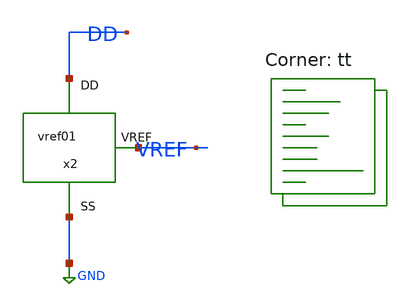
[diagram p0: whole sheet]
** sch_path: xschem/test_vref01.sch
**.subckt test_vref01
x2 VREF DD GND vref01
**** begin user architecture code
.lib $::SKYWATER_MODELS/sky130.lib.spice tt
**** end user architecture code
**.ends

* expanding   symbol:  vref01.sym # of pins=3
** sym_path: xschem/vref01.sym
** sch_path: xschem/vref01.sch
.subckt vref01 VREF DD SS
*.opin VREF
*.iopin SS
*.iopin DD
XM1 DD gate gate SS sky130_fd_pr__nfet_01v8_lvt L=0.89 W=6 nf=1 ad='int((nf+1)/2) * W/nf * 0.29' as='int((nf+2)/2) * W/nf * 0.29'
+ pd='2*int((nf+1)/2) * (W/nf + 0.29)' ps='2*int((nf+2)/2) * (W/nf + 0.29)' nrd='0.29 / W' nrs='0.29 / W'
+ sa=0 sb=0 sd=0 mult=2 m=2
XM2 gate gate VREF SS sky130_fd_pr__nfet_01v8_lvt L=3.10 W=1.72 nf=1 ad='int((nf+1)/2) * W/nf * 0.29'
+ as='int((nf+2)/2) * W/nf * 0.29' pd='2*int((nf+1)/2) * (W/nf + 0.29)' ps='2*int((nf+2)/2) * (W/nf + 0.29)'
+ nrd='0.29 / W' nrs='0.29 / W' sa=0 sb=0 sd=0 mult=1 m=1
XM3 VREF gate SS SS sky130_fd_pr__nfet_01v8 L=1.05 W=0.82 nf=1 ad='int((nf+1)/2) * W/nf * 0.29' as='int((nf+2)/2) * W/nf * 0.29'
+ pd='2*int((nf+1)/2) * (W/nf + 0.29)' ps='2*int((nf+2)/2) * (W/nf + 0.29)' nrd='0.29 / W' nrs='0.29 / W'
+ sa=0 sb=0 sd=0 mult=1 m=1
XM4 VREF VREF VREF DD sky130_fd_pr__pfet_01v8_lvt L=0.35 W=8.6 nf=1 ad='int((nf+1)/2) * W/nf * 1' as='int((nf+2)/2) * W/nf * 1'
+ pd='2*int((nf+1)/2) * (W/nf + 1)' ps='2*int((nf+2)/2) * (W/nf + 1)' nrd='1 / W' nrs='1 / W' sa=0 sb=0
+ sd=0 mult=1 m=1
.ends

.GLOBAL GND
**** begin user architecture code


** this experimental option enables mos model bin
** selection based on W/NF instead of W
*.option wnflag=1 savecurrents
.option gmin=1e-15 reltol=1e-3 vntol=1e-4 abstol=1e-14

.param vdd=1
v1 dd 0 dc=vdd


.control
  option seed = 8
  let run = 1
  save all
  op
  write test_vref01.raw
  reset
  set appendwrite
  dowhile run < = 1
    save vref i(v1)
    * save all
    dc temp -40 150 1
    write test_vref01.raw
    let run = run + 1
    reset
  end
  plot vref
.endc


**** end user architecture code
.end
